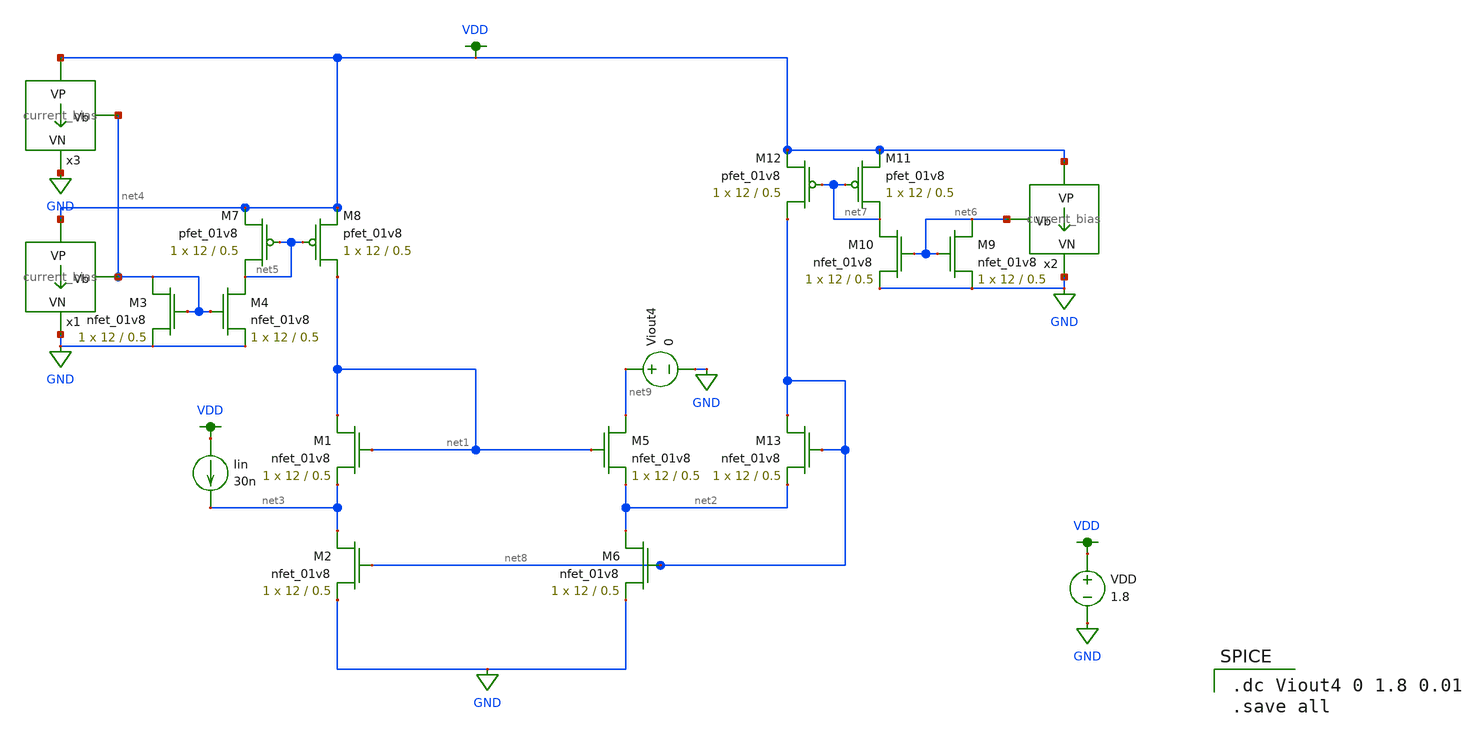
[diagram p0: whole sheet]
** sch_path: schematics/current mirrors/low_voltage_super_wilson_current_mirror.sch
**.subckt low_voltage_super_wilson_current_mirror
XM1 net1 net1 net3 GND sky130_fd_pr__nfet_01v8 L=0.5 W=12 nf=1 ad='int((nf+1)/2) * W/nf * 0.29' as='int((nf+2)/2) * W/nf * 0.29'
+ pd='2*int((nf+1)/2) * (W/nf + 0.29)' ps='2*int((nf+2)/2) * (W/nf + 0.29)' nrd='0.29 / W' nrs='0.29 / W'
+ sa=0 sb=0 sd=0 mult=1 m=1
XM2 net3 net8 GND GND sky130_fd_pr__nfet_01v8 L=0.5 W=12 nf=1 ad='int((nf+1)/2) * W/nf * 0.29' as='int((nf+2)/2) * W/nf * 0.29'
+ pd='2*int((nf+1)/2) * (W/nf + 0.29)' ps='2*int((nf+2)/2) * (W/nf + 0.29)' nrd='0.29 / W' nrs='0.29 / W'
+ sa=0 sb=0 sd=0 mult=1 m=1
XM5 net9 net1 net2 GND sky130_fd_pr__nfet_01v8 L=0.5 W=12 nf=1 ad='int((nf+1)/2) * W/nf * 0.29' as='int((nf+2)/2) * W/nf * 0.29'
+ pd='2*int((nf+1)/2) * (W/nf + 0.29)' ps='2*int((nf+2)/2) * (W/nf + 0.29)' nrd='0.29 / W' nrs='0.29 / W'
+ sa=0 sb=0 sd=0 mult=1 m=1
XM6 net2 net8 GND GND sky130_fd_pr__nfet_01v8 L=0.5 W=12 nf=1 ad='int((nf+1)/2) * W/nf * 0.29' as='int((nf+2)/2) * W/nf * 0.29'
+ pd='2*int((nf+1)/2) * (W/nf + 0.29)' ps='2*int((nf+2)/2) * (W/nf + 0.29)' nrd='0.29 / W' nrs='0.29 / W'
+ sa=0 sb=0 sd=0 mult=1 m=1
Viout4 net9 GND 0
Iin VDD net3 30n
VDD VDD GND 1.8
x1 VDD net4 GND current_bias
XM3 net4 net4 GND GND sky130_fd_pr__nfet_01v8 L=0.5 W=12 nf=1 ad='int((nf+1)/2) * W/nf * 0.29' as='int((nf+2)/2) * W/nf * 0.29'
+ pd='2*int((nf+1)/2) * (W/nf + 0.29)' ps='2*int((nf+2)/2) * (W/nf + 0.29)' nrd='0.29 / W' nrs='0.29 / W'
+ sa=0 sb=0 sd=0 mult=1 m=1
XM4 net5 net4 GND GND sky130_fd_pr__nfet_01v8 L=0.5 W=12 nf=1 ad='int((nf+1)/2) * W/nf * 0.29' as='int((nf+2)/2) * W/nf * 0.29'
+ pd='2*int((nf+1)/2) * (W/nf + 0.29)' ps='2*int((nf+2)/2) * (W/nf + 0.29)' nrd='0.29 / W' nrs='0.29 / W'
+ sa=0 sb=0 sd=0 mult=1 m=1
XM7 net5 net5 VDD VDD sky130_fd_pr__pfet_01v8 L=0.5 W=12 nf=1 ad='int((nf+1)/2) * W/nf * 0.29' as='int((nf+2)/2) * W/nf * 0.29'
+ pd='2*int((nf+1)/2) * (W/nf + 0.29)' ps='2*int((nf+2)/2) * (W/nf + 0.29)' nrd='0.29 / W' nrs='0.29 / W'
+ sa=0 sb=0 sd=0 mult=1 m=1
x2 VDD net6 GND current_bias
XM9 net6 net6 GND GND sky130_fd_pr__nfet_01v8 L=0.5 W=12 nf=1 ad='int((nf+1)/2) * W/nf * 0.29' as='int((nf+2)/2) * W/nf * 0.29'
+ pd='2*int((nf+1)/2) * (W/nf + 0.29)' ps='2*int((nf+2)/2) * (W/nf + 0.29)' nrd='0.29 / W' nrs='0.29 / W'
+ sa=0 sb=0 sd=0 mult=1 m=1
XM10 net7 net6 GND GND sky130_fd_pr__nfet_01v8 L=0.5 W=12 nf=1 ad='int((nf+1)/2) * W/nf * 0.29' as='int((nf+2)/2) * W/nf * 0.29'
+ pd='2*int((nf+1)/2) * (W/nf + 0.29)' ps='2*int((nf+2)/2) * (W/nf + 0.29)' nrd='0.29 / W' nrs='0.29 / W'
+ sa=0 sb=0 sd=0 mult=1 m=1
XM8 net1 net5 VDD VDD sky130_fd_pr__pfet_01v8 L=0.5 W=12 nf=1 ad='int((nf+1)/2) * W/nf * 0.29' as='int((nf+2)/2) * W/nf * 0.29'
+ pd='2*int((nf+1)/2) * (W/nf + 0.29)' ps='2*int((nf+2)/2) * (W/nf + 0.29)' nrd='0.29 / W' nrs='0.29 / W'
+ sa=0 sb=0 sd=0 mult=1 m=1
XM12 net8 net7 VDD VDD sky130_fd_pr__pfet_01v8 L=0.5 W=12 nf=1 ad='int((nf+1)/2) * W/nf * 0.29' as='int((nf+2)/2) * W/nf * 0.29'
+ pd='2*int((nf+1)/2) * (W/nf + 0.29)' ps='2*int((nf+2)/2) * (W/nf + 0.29)' nrd='0.29 / W' nrs='0.29 / W'
+ sa=0 sb=0 sd=0 mult=1 m=1
XM11 net7 net7 VDD VDD sky130_fd_pr__pfet_01v8 L=0.5 W=12 nf=1 ad='int((nf+1)/2) * W/nf * 0.29' as='int((nf+2)/2) * W/nf * 0.29'
+ pd='2*int((nf+1)/2) * (W/nf + 0.29)' ps='2*int((nf+2)/2) * (W/nf + 0.29)' nrd='0.29 / W' nrs='0.29 / W'
+ sa=0 sb=0 sd=0 mult=1 m=1
x3 VDD net4 GND current_bias
XM13 net8 net8 net2 GND sky130_fd_pr__nfet_01v8 L=0.5 W=12 nf=1 ad='int((nf+1)/2) * W/nf * 0.29' as='int((nf+2)/2) * W/nf * 0.29'
+ pd='2*int((nf+1)/2) * (W/nf + 0.29)' ps='2*int((nf+2)/2) * (W/nf + 0.29)' nrd='0.29 / W' nrs='0.29 / W'
+ sa=0 sb=0 sd=0 mult=1 m=1
**** begin user architecture code

.option wnflag=1
.param MC_SWITCH=0.0
.lib ~/skywater/skywater-pdk/libraries/sky130_fd_pr_ngspice/latest/models/sky130.lib.spice tt


.dc Viout4 0 1.8 0.01
.save all

**** end user architecture code
**.ends
.GLOBAL GND
.GLOBAL VDD
.end
